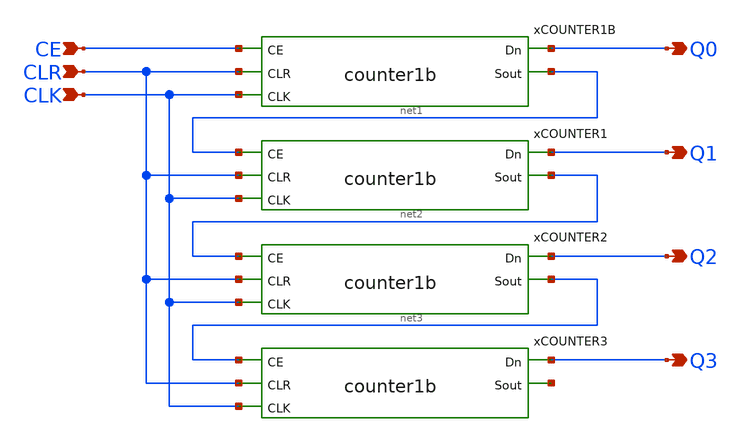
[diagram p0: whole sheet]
** sch_path: xschem/counter4b.sch
**.subckt counter4b CE CLR CLK Q0 Q1 Q2 Q3
*.ipin CE
*.ipin CLR
*.ipin CLK
*.opin Q0
*.opin Q1
*.opin Q2
*.opin Q3
xCOUNTER1B Q0 CE CLR CLK net1 VSS VDD counter1b
xCOUNTER1 Q1 net1 CLR CLK net2 VSS VDD counter1b
xCOUNTER2 Q2 net2 CLR CLK net3 VSS VDD counter1b
xCOUNTER3 Q3 net3 CLR CLK net4 VSS VDD counter1b
**.ends
.end
